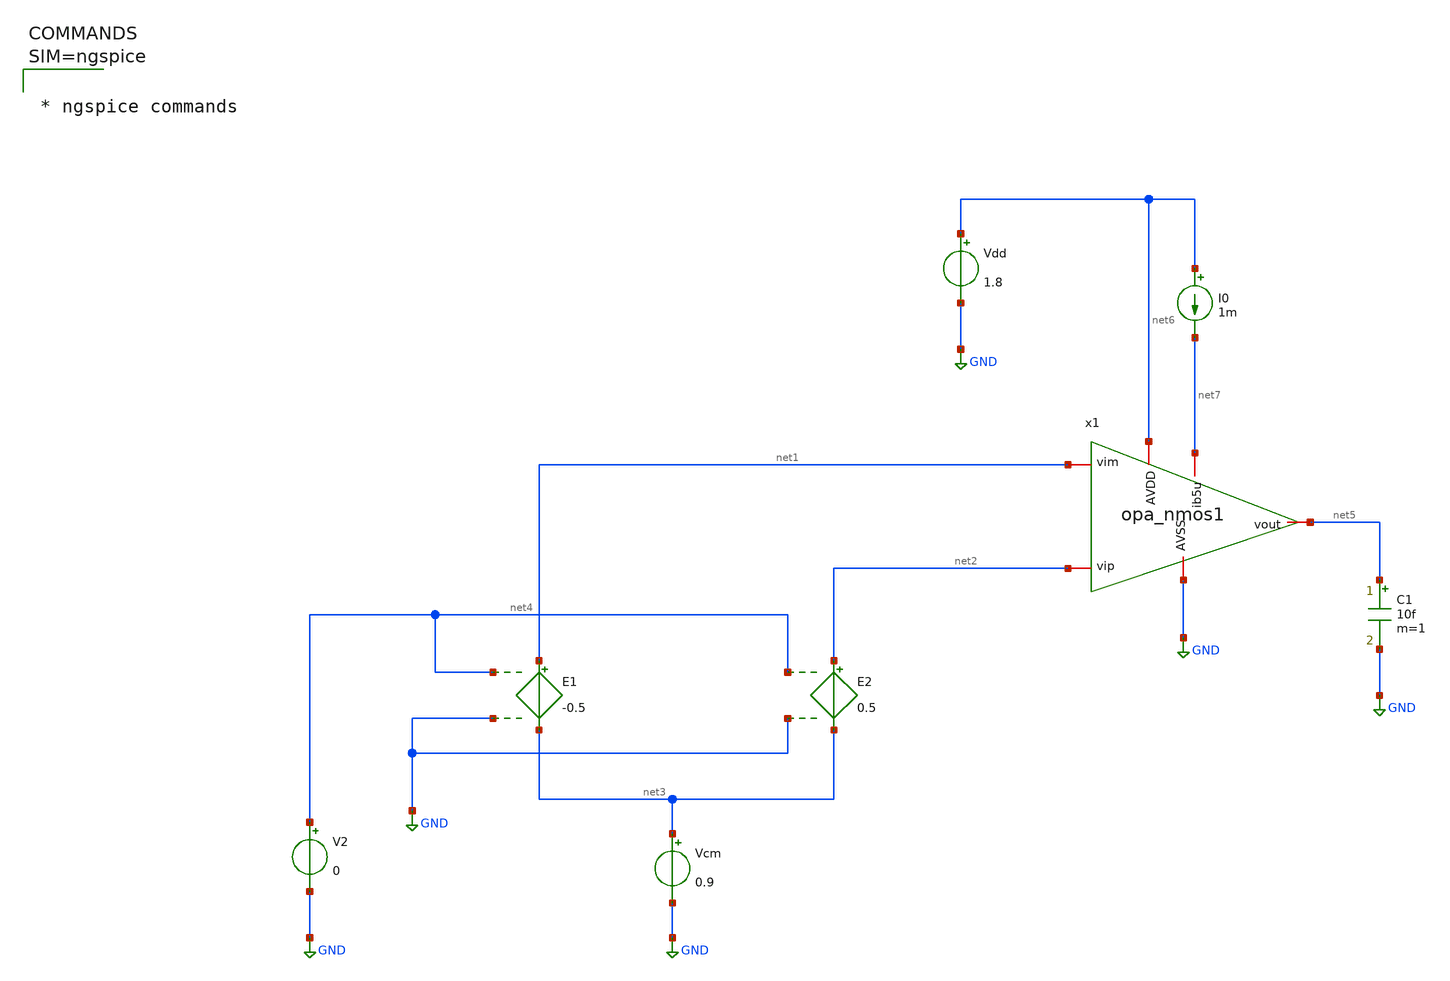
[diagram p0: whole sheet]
** sch_path: xschem/TB_opa_nmos1.sch
**.subckt TB_opa_nmos1
E2 net2 net3 net4 GND 0.5
E1 net1 net3 net4 GND -0.5
x1 net5 net2 GND net1 net6 net7 opa_nmos1
Vcm net3 GND 0.9
V2 net4 GND 0
C1 net5 GND 10f m=1
Vdd net6 GND 1.8
I0 net6 net7 1m
**** begin user architecture code

** opencircuitdesign pdks install
.lib $::SKYWATER_MODELS/sky130.lib.spice tt




* ngspice commands




**** end user architecture code
**.ends

* expanding   symbol:  opa_nmos1.sym # of pins=6
** sym_path: opa_nmos1.sym
** sch_path: opa_nmos1.sch
.subckt opa_nmos1 vout vip AVSS vim AVDD ib5u
*.iopin vip
*.iopin vim
*.iopin vout
*.iopin ib5u
*.iopin AVDD
*.iopin AVSS
XM1 ib5u ib5u AVSS AVSS sky130_fd_pr__nfet_01v8 L=1 W=5 nf=1 ad='int((1 + 1)/2) * 5 / 1 * 0.29' as='int((1 + 2)/2) * 5 / 1 * 0.29'
+ pd='2*int((1 + 1)/2) * (5 / 1 + 0.29)' ps='2*int((1 + 2)/2) * (5 / 1 + 0.29)' nrd='0.29 / 5 ' nrs='0.29 / 5 '
+ sa=0 sb=0 sd=0 mult=1 m=1
XM2 net3 ib5u AVSS AVSS sky130_fd_pr__nfet_01v8 L=1 W=5 nf=1 ad='int((1 + 1)/2) * 5 / 1 * 0.29' as='int((1 + 2)/2) * 5 / 1 * 0.29'
+ pd='2*int((1 + 1)/2) * (5 / 1 + 0.29)' ps='2*int((1 + 2)/2) * (5 / 1 + 0.29)' nrd='0.29 / 5 ' nrs='0.29 / 5 '
+ sa=0 sb=0 sd=0 mult=2 m=2
XM3 net1 net4 ib5u net5 sky130_fd_pr__nfet_01v8_lvt L=2 W=5 nf=1 ad='int((1 + 1)/2) * 5 / 1 * 0.29' as='int((1 + 2)/2) * 5 / 1 * 0.29'
+ pd='2*int((1 + 1)/2) * (5 / 1 + 0.29)' ps='2*int((1 + 2)/2) * (5 / 1 + 0.29)' nrd='0.29 / 5 ' nrs='0.29 / 5 '
+ sa=0 sb=0 sd=0 mult=4 m=4
XM4 vout net6 ib5u net7 sky130_fd_pr__nfet_01v8_lvt L=0.15 W=1 nf=1 ad='int((1 + 1)/2) * 1 / 1 * 0.29'
+ as='int((1 + 2)/2) * 1 / 1 * 0.29' pd='2*int((1 + 1)/2) * (1 / 1 + 0.29)' ps='2*int((1 + 2)/2) * (1 / 1 + 0.29)'
+ nrd='0.29 / 1 ' nrs='0.29 / 1 ' sa=0 sb=0 sd=0 mult=1 m=1
XM11 AVDD net2 net1 AVDD sky130_fd_pr__pfet_01v8 L=0.15 W=1 nf=1 ad='int((nf+1)/2) * W/nf * 0.29' as='int((nf+2)/2) * W/nf * 0.29'
+ pd='2*int((nf+1)/2) * (W/nf + 0.29)' ps='2*int((nf+2)/2) * (W/nf + 0.29)' nrd='0.29 / W' nrs='0.29 / W'
+ sa=0 sb=0 sd=0 mult=1 m=1
XM5 AVDD net2 vout AVDD sky130_fd_pr__pfet_01v8 L=0.15 W=1 nf=1 ad='int((nf+1)/2) * W/nf * 0.29' as='int((nf+2)/2) * W/nf * 0.29'
+ pd='2*int((nf+1)/2) * (W/nf + 0.29)' ps='2*int((nf+2)/2) * (W/nf + 0.29)' nrd='0.29 / W' nrs='0.29 / W'
+ sa=0 sb=0 sd=0 mult=1 m=1
.ends

.GLOBAL GND
.end
